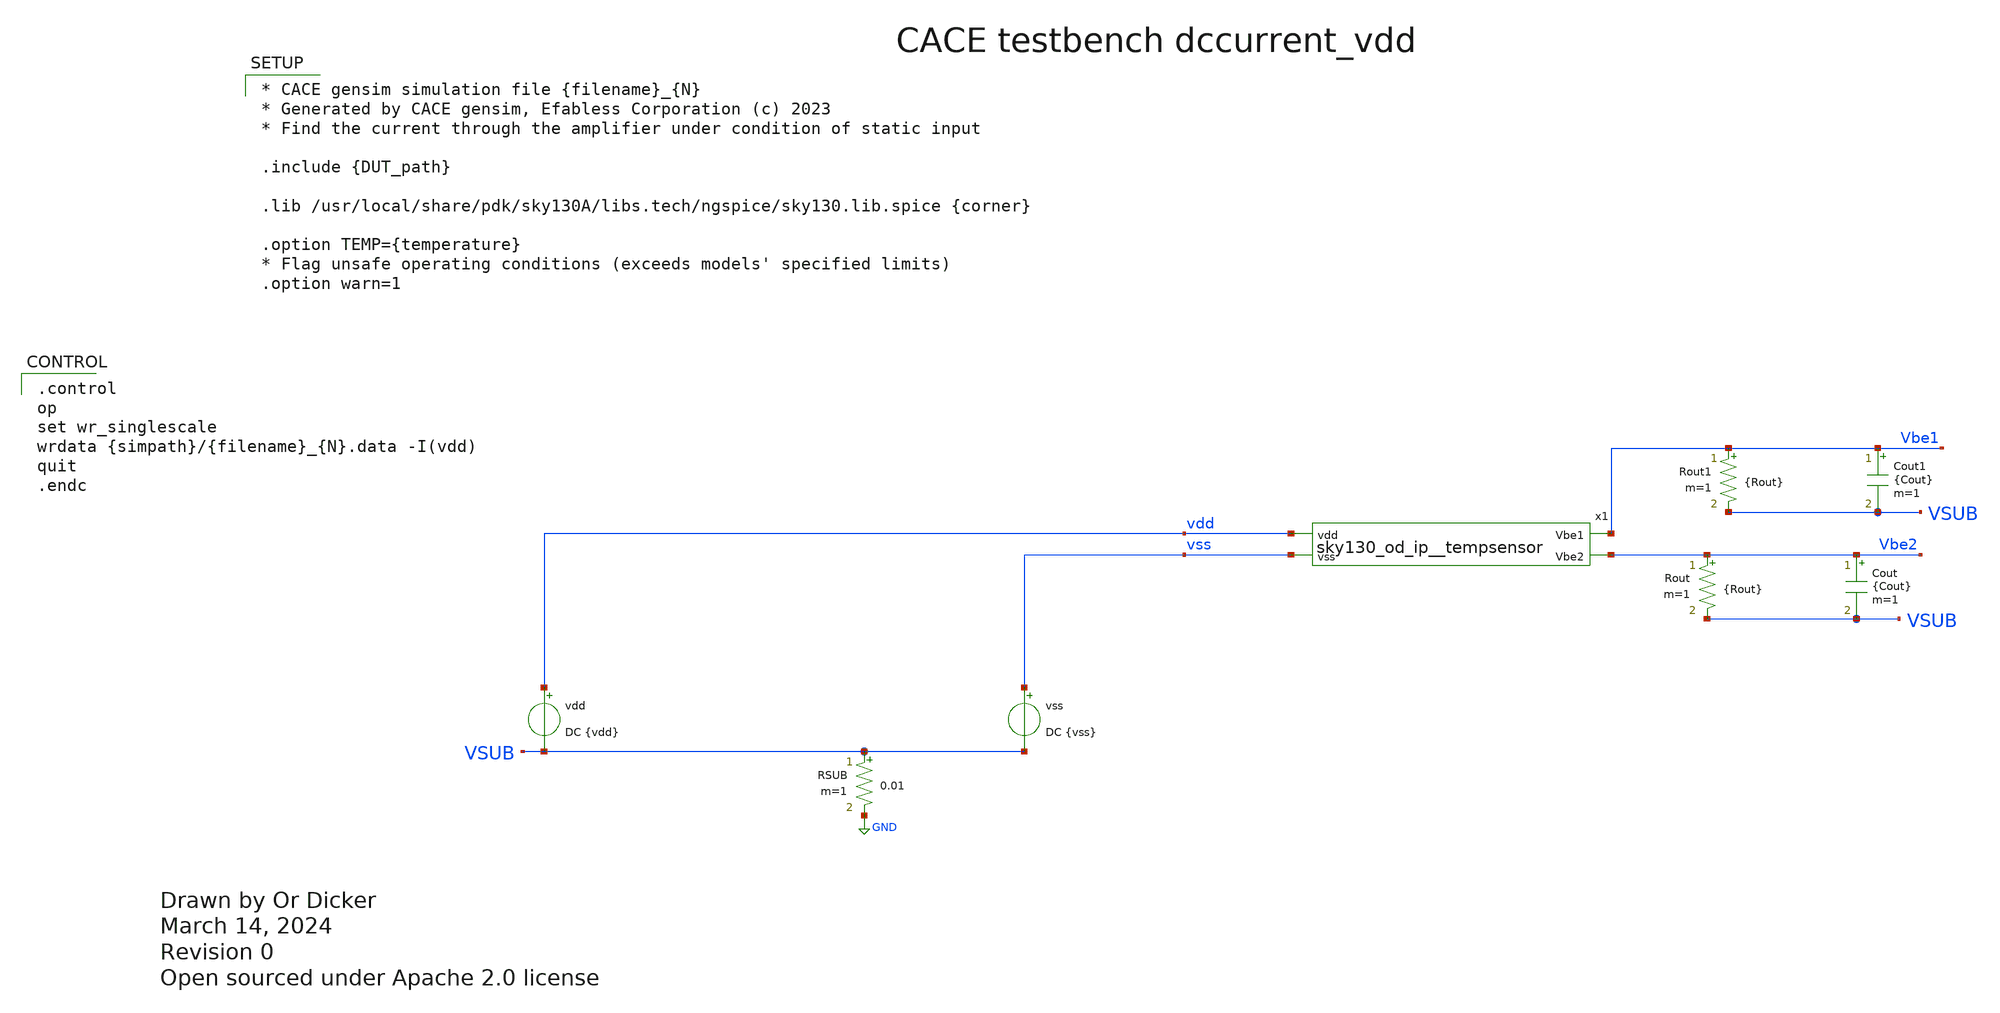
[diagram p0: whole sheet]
** sch_path: cace/dccurrent_vdd.sch
* Open sourced under Apache 2.0 license
**.subckt dccurrent_vdd
vss vss VSUB DC {vss}
Rout Vbe2 VSUB {Rout} m=1
Cout Vbe2 VSUB {Cout} m=1
vdd vdd VSUB DC {vdd}
RSUB VSUB GND 0.01 m=1
x1 vdd vss Vbe1 Vbe2 sky130_od_ip__tempsensor
Rout1 Vbe1 VSUB {Rout} m=1
Cout1 Vbe1 VSUB {Cout} m=1
**** begin user architecture code

.control
op
set wr_singlescale
wrdata {simpath}/{filename}_{N}.data -I(vdd)
quit
.endc



* CACE gensim simulation file {filename}_{N}
* Generated by CACE gensim, Efabless Corporation (c) 2023
* Find the current through the amplifier under condition of static input

.include {DUT_path}

.lib /usr/local/share/pdk/sky130A/libs.tech/ngspice/sky130.lib.spice {corner}

.option TEMP={temperature}
* Flag unsafe operating conditions (exceeds models' specified limits)
.option warn=1


**** end user architecture code
**.ends

* expanding   symbol:  xschem/sky130_od_ip__tempsensor.sym # of pins=4
** sym_path: xschem/sky130_od_ip__tempsensor.sym
** sch_path: xschem/sky130_od_ip__tempsensor.sch
.subckt sky130_od_ip__tempsensor vdd vss Vbe1 Vbe2
*.ipin vdd
*.ipin vss
*.opin Vbe2
*.opin Vbe1
XM12 net1 Vp vdd vdd sky130_fd_pr__pfet_01v8 L=0.15 W=5 nf=1 ad='int((nf+1)/2) * W/nf * 0.29' as='int((nf+2)/2)
+ * W/nf * 0.29' pd='2*int((nf+1)/2) * (W/nf + 0.29)' ps='2*int((nf+2)/2) * (W/nf + 0.29)' nrd='0.29 /
+ W' nrs='0.29 / W' sa=0 sb=0 sd=0 mult=1 m=1
XM13 net2 Vp vdd vdd sky130_fd_pr__pfet_01v8 L=0.15 W=1 nf=1 ad='int((nf+1)/2) * W/nf * 0.29' as='int((nf+2)/2)
+ * W/nf * 0.29' pd='2*int((nf+1)/2) * (W/nf + 0.29)' ps='2*int((nf+2)/2) * (W/nf + 0.29)' nrd='0.29 /
+ W' nrs='0.29 / W' sa=0 sb=0 sd=0 mult=1 m=1
XQ_BR vss net3 net1 sky130_fd_pr__pnp_05v5_W3p40L3p40 m=1
XQ_BL vss vss net4 sky130_fd_pr__pnp_05v5_W3p40L3p40 m=1
Rb net2 net4 1k m=1
Rb_5 net3 vss 0.2k m=1
XM11 net5 Vp vdd vdd sky130_fd_pr__pfet_01v8 L=0.15 W=2 nf=1 ad='int((nf+1)/2) * W/nf * 0.29' as='int((nf+2)/2)
+ * W/nf * 0.29' pd='2*int((nf+1)/2) * (W/nf + 0.29)' ps='2*int((nf+2)/2) * (W/nf + 0.29)' nrd='0.29 /
+ W' nrs='0.29 / W' sa=0 sb=0 sd=0 mult=1 m=1
XM6 net6 net2 net5 vdd sky130_fd_pr__pfet_01v8 L=0.15 W=1 nf=1 ad='int((nf+1)/2) * W/nf * 0.29' as='int((nf+2)/2)
+ * W/nf * 0.29' pd='2*int((nf+1)/2) * (W/nf + 0.29)' ps='2*int((nf+2)/2) * (W/nf + 0.29)' nrd='0.29 /
+ W' nrs='0.29 / W' sa=0 sb=0 sd=0 mult=1 m=1
XM5 net7 net1 net5 vdd sky130_fd_pr__pfet_01v8 L=0.15 W=5 nf=1 ad='int((nf+1)/2) * W/nf * 0.29' as='int((nf+2)/2)
+ * W/nf * 0.29' pd='2*int((nf+1)/2) * (W/nf + 0.29)' ps='2*int((nf+2)/2) * (W/nf + 0.29)' nrd='0.29 /
+ W' nrs='0.29 / W' sa=0 sb=0 sd=0 mult=1 m=1
XM2 net6 net6 vss vss sky130_fd_pr__nfet_01v8 L=0.15 W=1 nf=1 ad='int((nf+1)/2) * W/nf * 0.29' as='int((nf+2)/2)
+ * W/nf * 0.29' pd='2*int((nf+1)/2) * (W/nf + 0.29)' ps='2*int((nf+2)/2) * (W/nf + 0.29)' nrd='0.29 /
+ W' nrs='0.29 / W' sa=0 sb=0 sd=0 mult=1 m=1
XM1 net7 net7 vss vss sky130_fd_pr__nfet_01v8 L=0.15 W=1 nf=1 ad='int((nf+1)/2) * W/nf * 0.29' as='int((nf+2)/2)
+ * W/nf * 0.29' pd='2*int((nf+1)/2) * (W/nf + 0.29)' ps='2*int((nf+2)/2) * (W/nf + 0.29)' nrd='0.29 /
+ W' nrs='0.29 / W' sa=0 sb=0 sd=0 mult=1 m=1
XM9 net8 Vp vdd vdd sky130_fd_pr__pfet_01v8 L=0.15 W=1 nf=1 ad='int((nf+1)/2) * W/nf * 0.29' as='int((nf+2)/2)
+ * W/nf * 0.29' pd='2*int((nf+1)/2) * (W/nf + 0.29)' ps='2*int((nf+2)/2) * (W/nf + 0.29)' nrd='0.29 /
+ W' nrs='0.29 / W' sa=0 sb=0 sd=0 mult=1 m=1
XM10 Vp Vp vdd vdd sky130_fd_pr__pfet_01v8 L=0.15 W=4 nf=1 ad='int((nf+1)/2) * W/nf * 0.29' as='int((nf+2)/2)
+ * W/nf * 0.29' pd='2*int((nf+1)/2) * (W/nf + 0.29)' ps='2*int((nf+2)/2) * (W/nf + 0.29)' nrd='0.29 /
+ W' nrs='0.29 / W' sa=0 sb=0 sd=0 mult=1 m=1
XM7 Vp net8 net10 vss sky130_fd_pr__nfet_01v8 L=0.15 W=1 nf=1 ad='int((nf+1)/2) * W/nf * 0.29' as='int((nf+2)/2)
+ * W/nf * 0.29' pd='2*int((nf+1)/2) * (W/nf + 0.29)' ps='2*int((nf+2)/2) * (W/nf + 0.29)' nrd='0.29 /
+ W' nrs='0.29 / W' sa=0 sb=0 sd=0 mult=1 m=1
XM8 net8 net8 net9 vss sky130_fd_pr__nfet_01v8 L=0.15 W=1 nf=1 ad='int((nf+1)/2) * W/nf * 0.29' as='int((nf+2)/2)
+ * W/nf * 0.29' pd='2*int((nf+1)/2) * (W/nf + 0.29)' ps='2*int((nf+2)/2) * (W/nf + 0.29)' nrd='0.29 /
+ W' nrs='0.29 / W' sa=0 sb=0 sd=0 mult=1 m=1
XM3 net10 net6 vss vss sky130_fd_pr__nfet_01v8 L=0.15 W=1 nf=1 ad='int((nf+1)/2) * W/nf * 0.29' as='int((nf+2)/2)
+ * W/nf * 0.29' pd='2*int((nf+1)/2) * (W/nf + 0.29)' ps='2*int((nf+2)/2) * (W/nf + 0.29)' nrd='0.29 /
+ W' nrs='0.29 / W' sa=0 sb=0 sd=0 mult=1 m=1
XM4 net9 net9 vss vss sky130_fd_pr__nfet_01v8 L=0.15 W=1 nf=1 ad='int((nf+1)/2) * W/nf * 0.29' as='int((nf+2)/2)
+ * W/nf * 0.29' pd='2*int((nf+1)/2) * (W/nf + 0.29)' ps='2*int((nf+2)/2) * (W/nf + 0.29)' nrd='0.29 /
+ W' nrs='0.29 / W' sa=0 sb=0 sd=0 mult=1 m=1
XQ_BL1 vss vss Vbe1 sky130_fd_pr__pnp_05v5_W3p40L3p40 m=1
XQ_BR1 vss vss Vbe2 sky130_fd_pr__pnp_05v5_W3p40L3p40 m=1
XM14 Vbe1 Vp vdd vdd sky130_fd_pr__pfet_01v8 L=0.15 W=2 nf=1 ad='int((nf+1)/2) * W/nf * 0.29' as='int((nf+2)/2)
+ * W/nf * 0.29' pd='2*int((nf+1)/2) * (W/nf + 0.29)' ps='2*int((nf+2)/2) * (W/nf + 0.29)' nrd='0.29 /
+ W' nrs='0.29 / W' sa=0 sb=0 sd=0 mult=1 m=1
XM15 Vbe2 Vp vdd vdd sky130_fd_pr__pfet_01v8 L=0.15 W=10 nf=1 ad='int((nf+1)/2) * W/nf * 0.29' as='int((nf+2)/2)
+ * W/nf * 0.29' pd='2*int((nf+1)/2) * (W/nf + 0.29)' ps='2*int((nf+2)/2) * (W/nf + 0.29)' nrd='0.29 /
+ W' nrs='0.29 / W' sa=0 sb=0 sd=0 mult=1 m=1
.ends

.GLOBAL GND
.end
